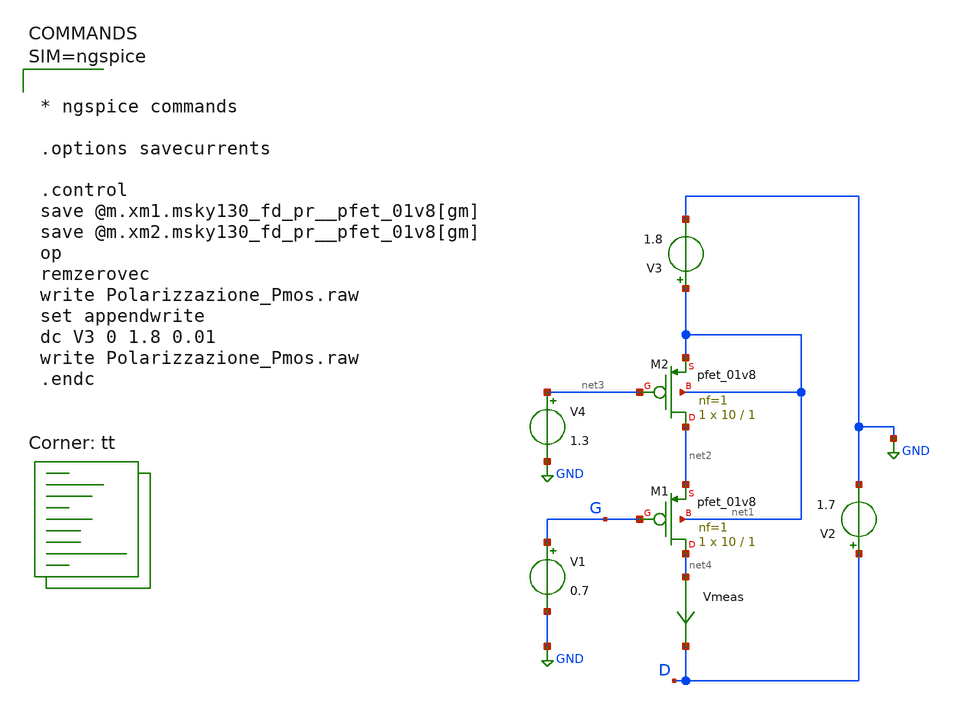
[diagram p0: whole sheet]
** sch_path: xschem/Polarizzazione_Pmos.sch
* Copyright 2021 Stefan Frederik Schippers
* Licensed under the Apache License, Version 2.0 (the "License");
* you may not use this file except in compliance with the License.
* You may obtain a copy of the License at
* https://www.apache.org/licenses/LICENSE-2.0
* Unless required by applicable law or agreed to in writing, software
* distributed under the License is distributed on an "AS IS" BASIS,
* WITHOUT WARRANTIES OR CONDITIONS OF ANY KIND, either express or implied.
* See the License for the specific language governing permissions and
* limitations under the License.
**.subckt Polarizzazione_Pmos
V1 G GND 0.7
V2 D GND 1.7
XM1 net4 G net2 net1 sky130_fd_pr__pfet_01v8 L=1 W=10 nf=1 ad='int((nf+1)/2) * W/nf * 0.29' as='int((nf+2)/2) * W/nf * 0.29'
+ pd='2*int((nf+1)/2) * (W/nf + 0.29)' ps='2*int((nf+2)/2) * (W/nf + 0.29)' nrd='0.29 / W' nrs='0.29 / W'
+ sa=0 sb=0 sd=0 mult=1 m=1
V3 net1 GND 1.8
XM2 net2 net3 net1 net1 sky130_fd_pr__pfet_01v8 L=1 W=10 nf=1 ad='int((nf+1)/2) * W/nf * 0.29' as='int((nf+2)/2) * W/nf * 0.29'
+ pd='2*int((nf+1)/2) * (W/nf + 0.29)' ps='2*int((nf+2)/2) * (W/nf + 0.29)' nrd='0.29 / W' nrs='0.29 / W'
+ sa=0 sb=0 sd=0 mult=1 m=1
V4 net3 GND 1.3
Vmeas net4 D 0
.save i(vmeas)
**** begin user architecture code



* ngspice commands

.options savecurrents

.control
save @m.xm1.msky130_fd_pr__pfet_01v8[gm]
save @m.xm2.msky130_fd_pr__pfet_01v8[gm]
op
remzerovec
write Polarizzazione_Pmos.raw
set appendwrite
dc V3 0 1.8 0.01
write Polarizzazione_Pmos.raw
.endc



.lib $::SKYWATER_MODELS/sky130.lib.spice tt
**** end user architecture code
**.ends
.GLOBAL GND
.end
